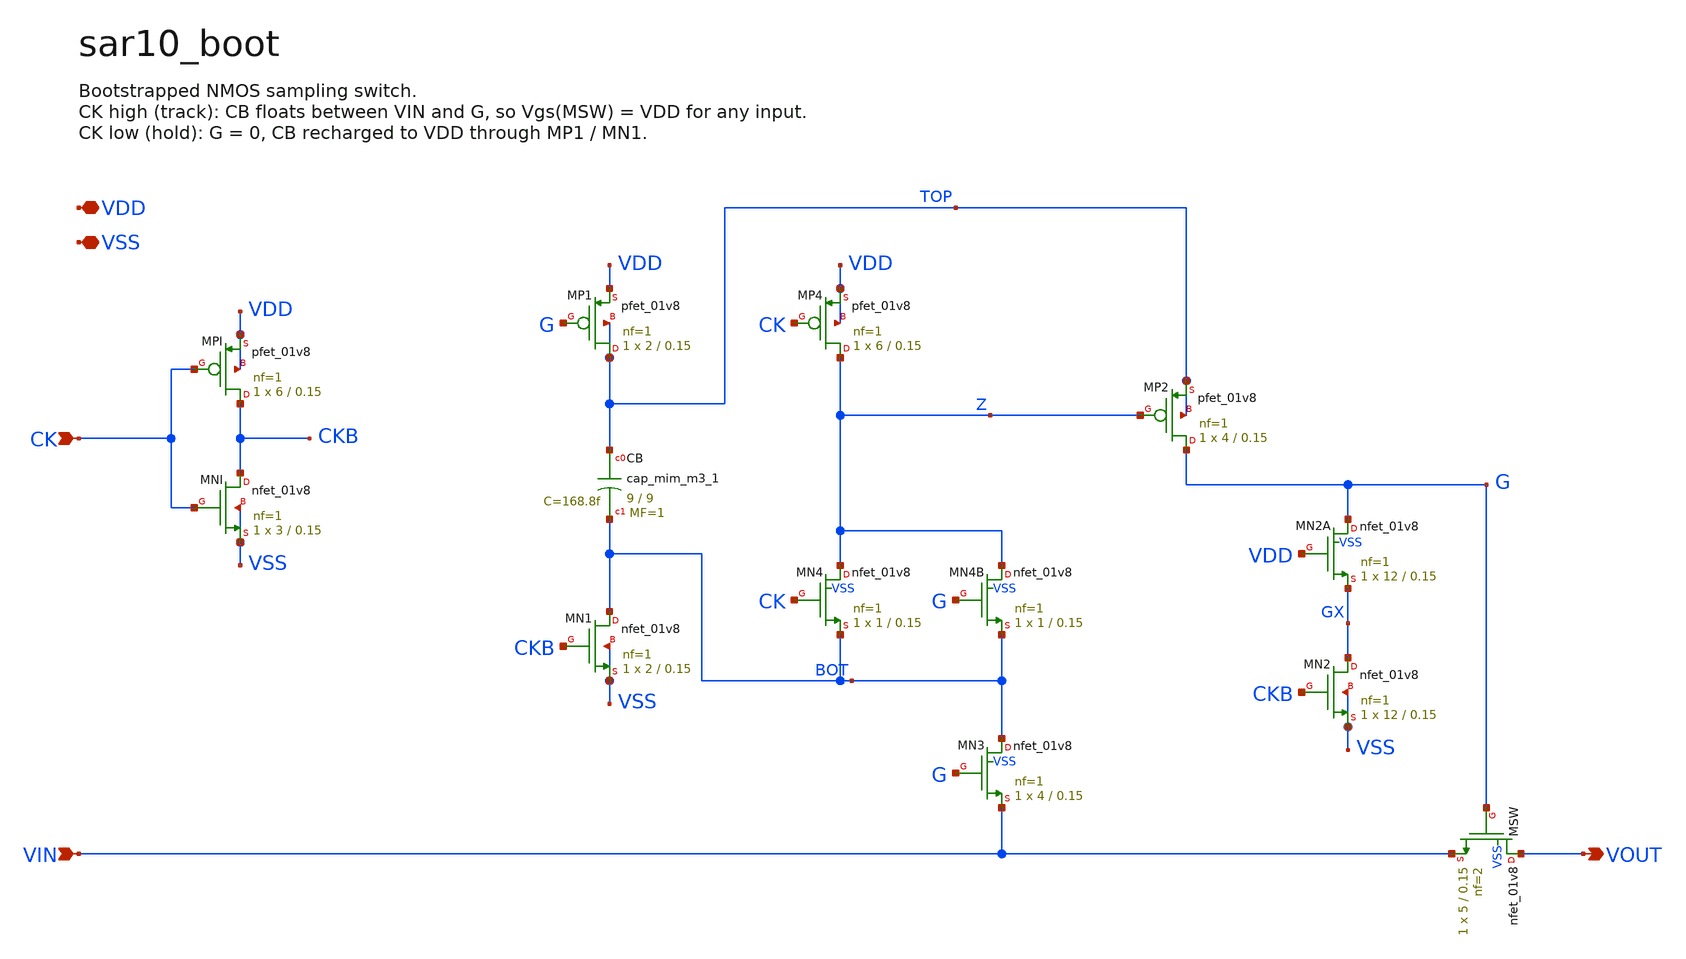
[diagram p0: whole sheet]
** sch_path: xschem/sar10_boot.sch
**.subckt sar10_boot CK VIN VOUT VDD VSS
*.ipin CK
*.ipin VIN
*.opin VOUT
*.iopin VDD
*.iopin VSS
XMPI CKB CK VDD VDD sky130_fd_pr__pfet_01v8 L=0.15 W=6 nf=1 ad='int((1 + 1)/2) * 6 / 1 * 0.29' as='int((1 + 2)/2) * 6 / 1 * 0.29'
+ pd='2*int((1 + 1)/2) * (6 / 1 + 0.29)' ps='2*int((1 + 2)/2) * (6 / 1 + 0.29)' nrd='0.29 / 6 ' nrs='0.29 / 6 '
+ sa=0 sb=0 sd=0 mult=1 m=1
XMNI CKB CK VSS VSS sky130_fd_pr__nfet_01v8 L=0.15 W=3 nf=1 ad='int((1 + 1)/2) * 3 / 1 * 0.29' as='int((1 + 2)/2) * 3 / 1 * 0.29'
+ pd='2*int((1 + 1)/2) * (3 / 1 + 0.29)' ps='2*int((1 + 2)/2) * (3 / 1 + 0.29)' nrd='0.29 / 3 ' nrs='0.29 / 3 '
+ sa=0 sb=0 sd=0 mult=1 m=1
XMP1 TOP G VDD TOP sky130_fd_pr__pfet_01v8 L=0.15 W=2 nf=1 ad='int((1 + 1)/2) * 2 / 1 * 0.29' as='int((1 + 2)/2) * 2 / 1 * 0.29'
+ pd='2*int((1 + 1)/2) * (2 / 1 + 0.29)' ps='2*int((1 + 2)/2) * (2 / 1 + 0.29)' nrd='0.29 / 2 ' nrs='0.29 / 2 '
+ sa=0 sb=0 sd=0 mult=1 m=1
XCB TOP BOT sky130_fd_pr__cap_mim_m3_1 W=9 L=9 MF=1 m=1
XMN1 BOT CKB VSS VSS sky130_fd_pr__nfet_01v8 L=0.15 W=2 nf=1 ad='int((1 + 1)/2) * 2 / 1 * 0.29' as='int((1 + 2)/2) * 2 / 1 * 0.29'
+ pd='2*int((1 + 1)/2) * (2 / 1 + 0.29)' ps='2*int((1 + 2)/2) * (2 / 1 + 0.29)' nrd='0.29 / 2 ' nrs='0.29 / 2 '
+ sa=0 sb=0 sd=0 mult=1 m=1
XMP4 Z CK VDD VDD sky130_fd_pr__pfet_01v8 L=0.15 W=6 nf=1 ad='int((1 + 1)/2) * 6 / 1 * 0.29' as='int((1 + 2)/2) * 6 / 1 * 0.29'
+ pd='2*int((1 + 1)/2) * (6 / 1 + 0.29)' ps='2*int((1 + 2)/2) * (6 / 1 + 0.29)' nrd='0.29 / 6 ' nrs='0.29 / 6 '
+ sa=0 sb=0 sd=0 mult=1 m=1
XMN4 Z CK BOT VSS sky130_fd_pr__nfet_01v8 L=0.15 W=1 nf=1 ad='int((1 + 1)/2) * 1 / 1 * 0.29' as='int((1 + 2)/2) * 1 / 1 * 0.29'
+ pd='2*int((1 + 1)/2) * (1 / 1 + 0.29)' ps='2*int((1 + 2)/2) * (1 / 1 + 0.29)' nrd='0.29 / 1 ' nrs='0.29 / 1 '
+ sa=0 sb=0 sd=0 mult=1 m=1
XMN4B Z G BOT VSS sky130_fd_pr__nfet_01v8 L=0.15 W=1 nf=1 ad='int((1 + 1)/2) * 1 / 1 * 0.29' as='int((1 + 2)/2) * 1 / 1 * 0.29'
+ pd='2*int((1 + 1)/2) * (1 / 1 + 0.29)' ps='2*int((1 + 2)/2) * (1 / 1 + 0.29)' nrd='0.29 / 1 ' nrs='0.29 / 1 '
+ sa=0 sb=0 sd=0 mult=1 m=1
XMP2 G Z TOP TOP sky130_fd_pr__pfet_01v8 L=0.15 W=4 nf=1 ad='int((1 + 1)/2) * 4 / 1 * 0.29' as='int((1 + 2)/2) * 4 / 1 * 0.29'
+ pd='2*int((1 + 1)/2) * (4 / 1 + 0.29)' ps='2*int((1 + 2)/2) * (4 / 1 + 0.29)' nrd='0.29 / 4 ' nrs='0.29 / 4 '
+ sa=0 sb=0 sd=0 mult=1 m=1
XMN3 BOT G VIN VSS sky130_fd_pr__nfet_01v8 L=0.15 W=4 nf=1 ad='int((1 + 1)/2) * 4 / 1 * 0.29' as='int((1 + 2)/2) * 4 / 1 * 0.29'
+ pd='2*int((1 + 1)/2) * (4 / 1 + 0.29)' ps='2*int((1 + 2)/2) * (4 / 1 + 0.29)' nrd='0.29 / 4 ' nrs='0.29 / 4 '
+ sa=0 sb=0 sd=0 mult=1 m=1
XMN2A G VDD GX VSS sky130_fd_pr__nfet_01v8 L=0.15 W=12 nf=1 ad='int((1 + 1)/2) * 12 / 1 * 0.29' as='int((1 + 2)/2) * 12 / 1 * 0.29'
+ pd='2*int((1 + 1)/2) * (12 / 1 + 0.29)' ps='2*int((1 + 2)/2) * (12 / 1 + 0.29)' nrd='0.29 / 12 ' nrs='0.29 / 12 '
+ sa=0 sb=0 sd=0 mult=1 m=1
XMN2 GX CKB VSS VSS sky130_fd_pr__nfet_01v8 L=0.15 W=12 nf=1 ad='int((1 + 1)/2) * 12 / 1 * 0.29' as='int((1 + 2)/2) * 12 / 1 * 0.29'
+ pd='2*int((1 + 1)/2) * (12 / 1 + 0.29)' ps='2*int((1 + 2)/2) * (12 / 1 + 0.29)' nrd='0.29 / 12 ' nrs='0.29 / 12 '
+ sa=0 sb=0 sd=0 mult=1 m=1
XMSW VOUT G VIN VSS sky130_fd_pr__nfet_01v8 L=0.15 W=5 nf=2 ad='int((2 + 1)/2) * 5 / 2 * 0.29' as='int((2 + 2)/2) * 5 / 2 * 0.29'
+ pd='2*int((2 + 1)/2) * (5 / 2 + 0.29)' ps='2*int((2 + 2)/2) * (5 / 2 + 0.29)' nrd='0.29 / 5 ' nrs='0.29 / 5 '
+ sa=0 sb=0 sd=0 mult=1 m=1
**.ends
.end
